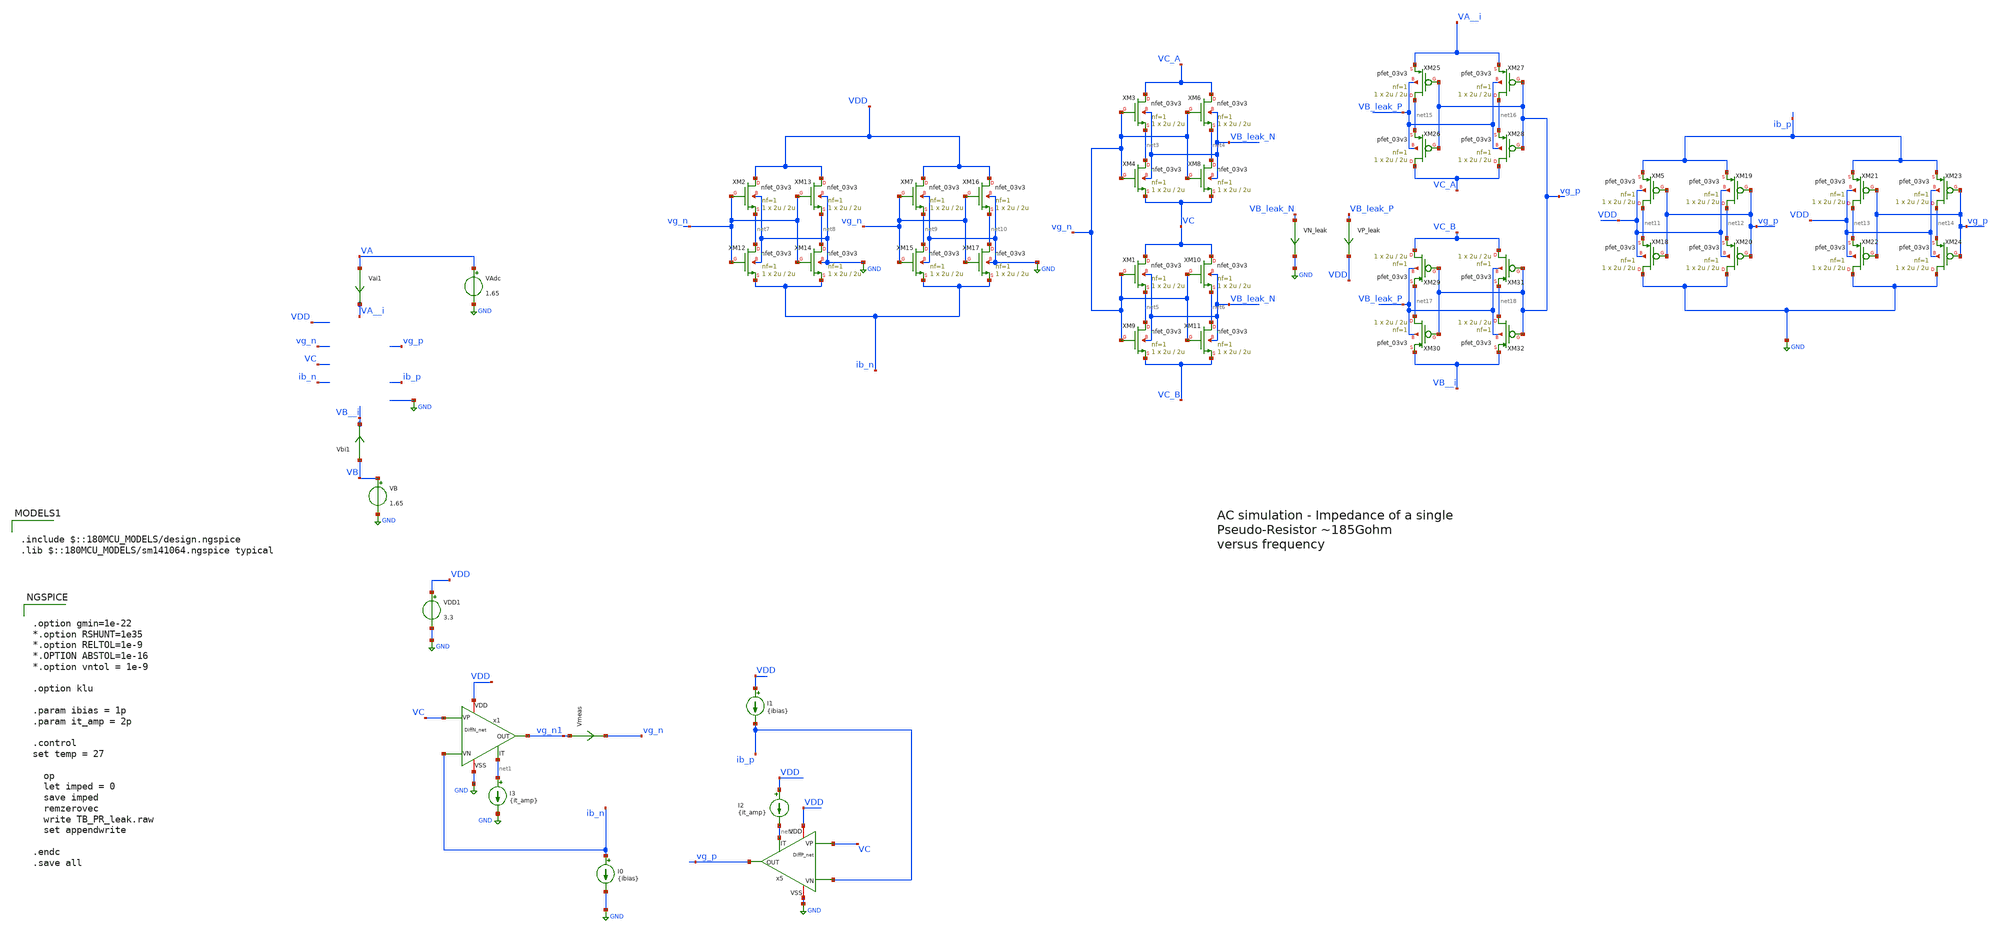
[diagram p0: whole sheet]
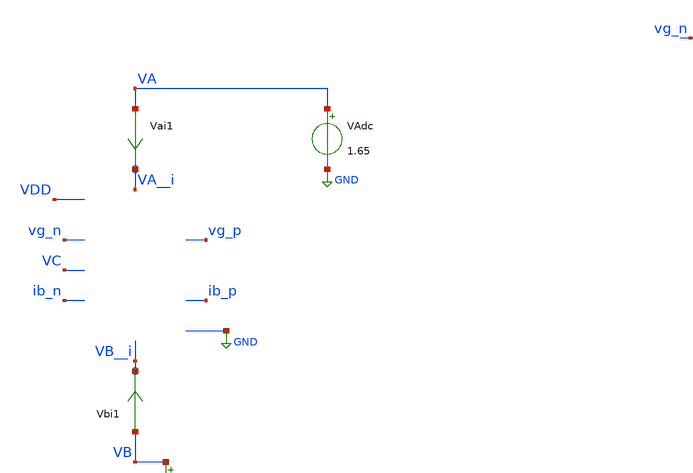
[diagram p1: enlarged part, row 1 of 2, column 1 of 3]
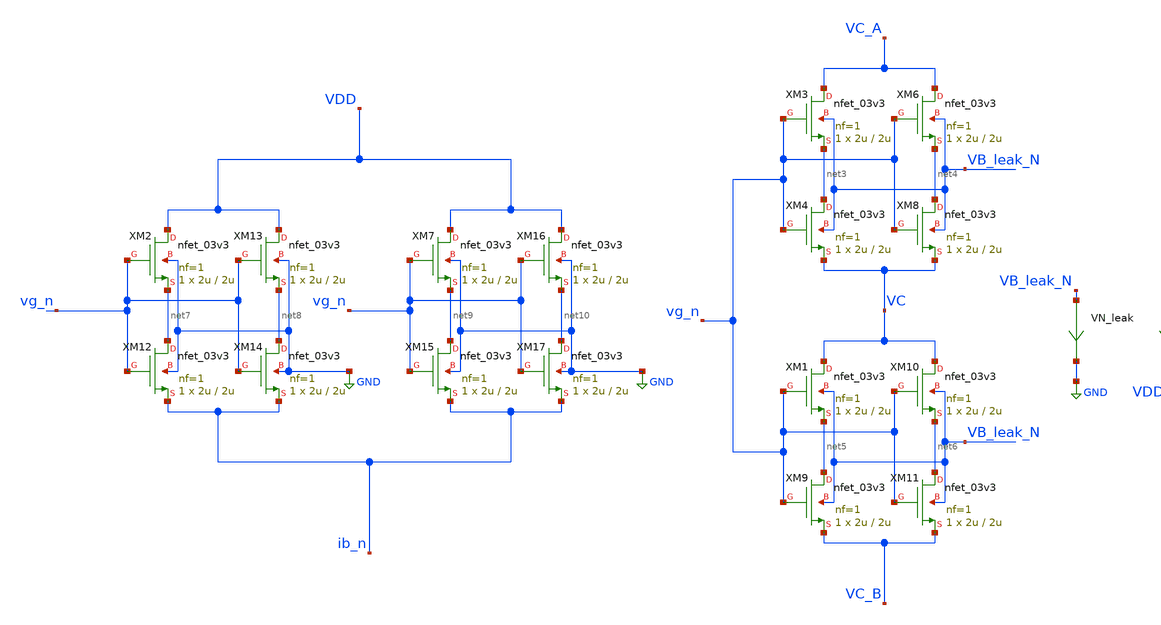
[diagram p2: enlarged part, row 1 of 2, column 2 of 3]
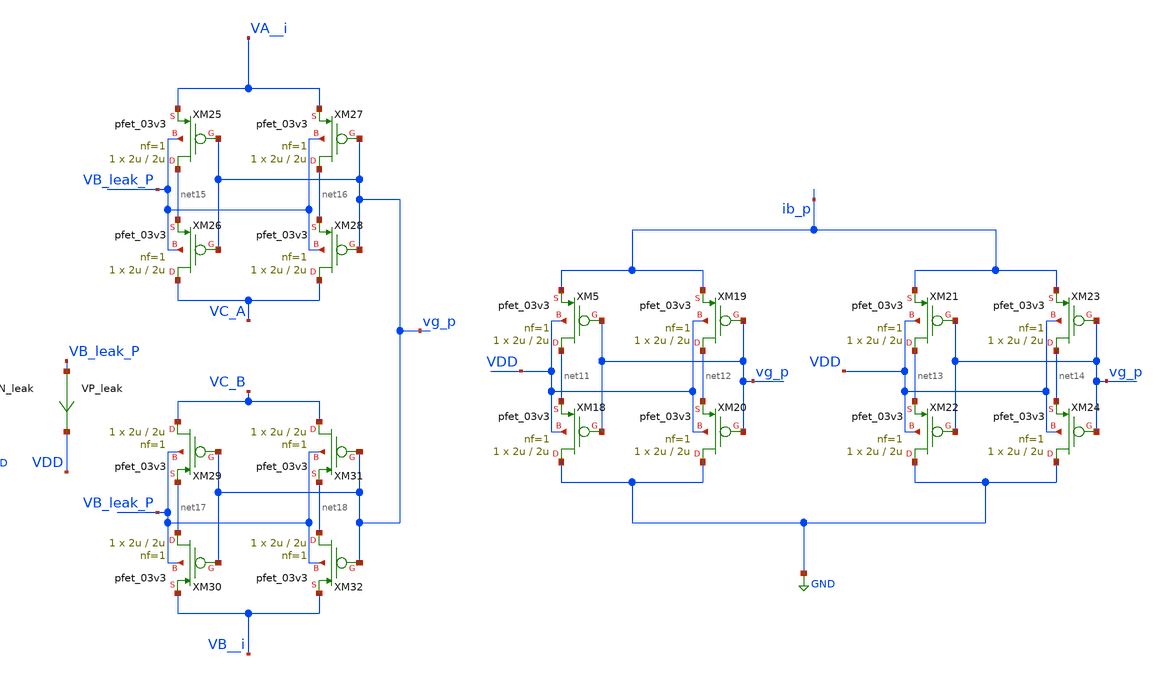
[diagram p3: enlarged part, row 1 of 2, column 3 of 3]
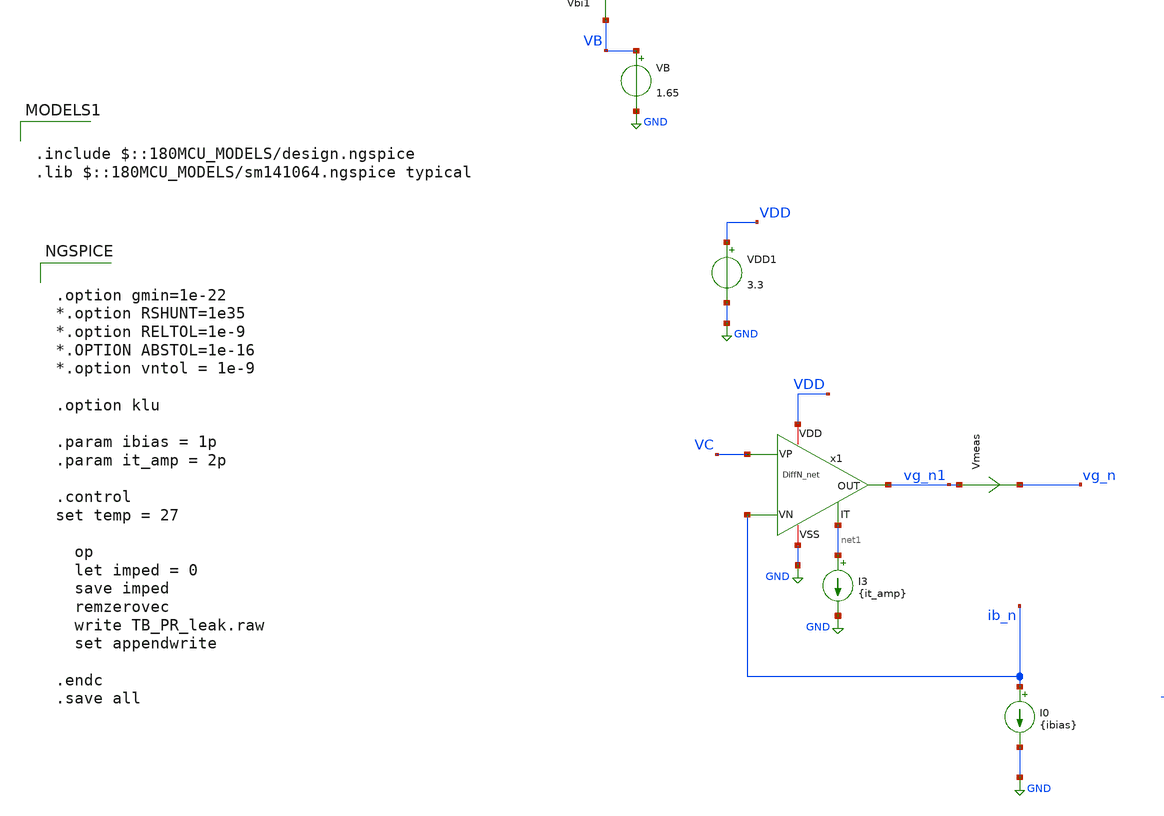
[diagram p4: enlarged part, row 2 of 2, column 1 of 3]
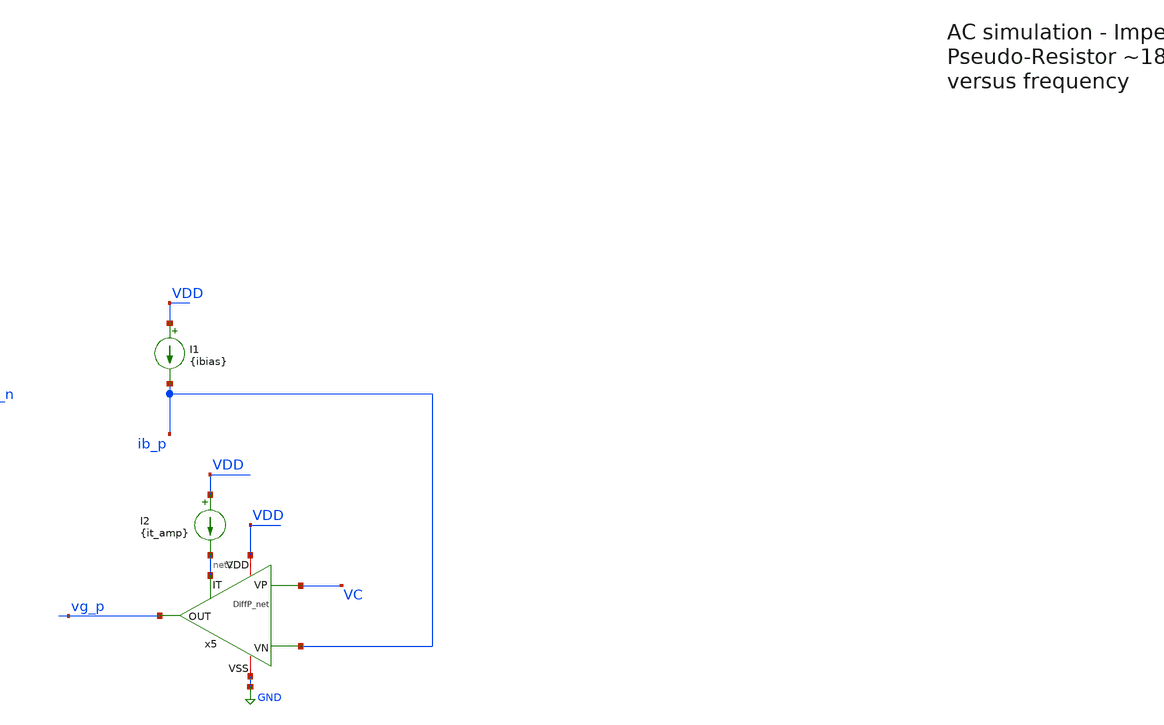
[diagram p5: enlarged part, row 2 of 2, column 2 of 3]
** sch_path: TIA_Filter/PseudoResistor/TB_PR_leak.sch
**.subckt TB_PR_leak
VDD1 VDD GND 3.3
VB VB GND 1.65
VAdc VA GND 1.65
Vai1 VA VA__i 0
.save i(vai1)
Vbi1 VB VB__i 0
.save i(vbi1)
I0 ib_n GND {ibias}
I1 VDD ib_p {ibias}
I2 VDD net2 {it_amp}
I3 net1 GND {it_amp}
x1 ib_n VC vg_n1 net1 VDD GND DiffN_net
x5 ib_p VC vg_p net2 VDD GND DiffP_net
XM3 VC_A vg_n net3 VB_leak_N nfet_03v3 L=2u W=2u nf=1 ad='int((nf+1)/2) * W/nf * 0.18u' as='int((nf+2)/2) * W/nf * 0.18u'
+ pd='2*int((nf+1)/2) * (W/nf + 0.18u)' ps='2*int((nf+2)/2) * (W/nf + 0.18u)' nrd='0.18u / W' nrs='0.18u / W'
+ sa=0 sb=0 sd=0 m=1
XM4 net3 vg_n VC VB_leak_N nfet_03v3 L=2u W=2u nf=1 ad='int((nf+1)/2) * W/nf * 0.18u' as='int((nf+2)/2) * W/nf * 0.18u'
+ pd='2*int((nf+1)/2) * (W/nf + 0.18u)' ps='2*int((nf+2)/2) * (W/nf + 0.18u)' nrd='0.18u / W' nrs='0.18u / W'
+ sa=0 sb=0 sd=0 m=1
XM6 VC_A vg_n net4 VB_leak_N nfet_03v3 L=2u W=2u nf=1 ad='int((nf+1)/2) * W/nf * 0.18u' as='int((nf+2)/2) * W/nf * 0.18u'
+ pd='2*int((nf+1)/2) * (W/nf + 0.18u)' ps='2*int((nf+2)/2) * (W/nf + 0.18u)' nrd='0.18u / W' nrs='0.18u / W'
+ sa=0 sb=0 sd=0 m=1
XM8 net4 vg_n VC VB_leak_N nfet_03v3 L=2u W=2u nf=1 ad='int((nf+1)/2) * W/nf * 0.18u' as='int((nf+2)/2) * W/nf * 0.18u'
+ pd='2*int((nf+1)/2) * (W/nf + 0.18u)' ps='2*int((nf+2)/2) * (W/nf + 0.18u)' nrd='0.18u / W' nrs='0.18u / W'
+ sa=0 sb=0 sd=0 m=1
XM1 VC vg_n net5 VB_leak_N nfet_03v3 L=2u W=2u nf=1 ad='int((nf+1)/2) * W/nf * 0.18u' as='int((nf+2)/2) * W/nf * 0.18u'
+ pd='2*int((nf+1)/2) * (W/nf + 0.18u)' ps='2*int((nf+2)/2) * (W/nf + 0.18u)' nrd='0.18u / W' nrs='0.18u / W'
+ sa=0 sb=0 sd=0 m=1
XM9 net5 vg_n VC_B VB_leak_N nfet_03v3 L=2u W=2u nf=1 ad='int((nf+1)/2) * W/nf * 0.18u' as='int((nf+2)/2) * W/nf * 0.18u'
+ pd='2*int((nf+1)/2) * (W/nf + 0.18u)' ps='2*int((nf+2)/2) * (W/nf + 0.18u)' nrd='0.18u / W' nrs='0.18u / W'
+ sa=0 sb=0 sd=0 m=1
XM10 VC vg_n net6 VB_leak_N nfet_03v3 L=2u W=2u nf=1 ad='int((nf+1)/2) * W/nf * 0.18u' as='int((nf+2)/2) * W/nf * 0.18u'
+ pd='2*int((nf+1)/2) * (W/nf + 0.18u)' ps='2*int((nf+2)/2) * (W/nf + 0.18u)' nrd='0.18u / W' nrs='0.18u / W'
+ sa=0 sb=0 sd=0 m=1
XM11 net6 vg_n VC_B VB_leak_N nfet_03v3 L=2u W=2u nf=1 ad='int((nf+1)/2) * W/nf * 0.18u' as='int((nf+2)/2) * W/nf * 0.18u'
+ pd='2*int((nf+1)/2) * (W/nf + 0.18u)' ps='2*int((nf+2)/2) * (W/nf + 0.18u)' nrd='0.18u / W' nrs='0.18u / W'
+ sa=0 sb=0 sd=0 m=1
XM2 VDD vg_n net7 GND nfet_03v3 L=2u W=2u nf=1 ad='int((nf+1)/2) * W/nf * 0.18u' as='int((nf+2)/2) * W/nf * 0.18u'
+ pd='2*int((nf+1)/2) * (W/nf + 0.18u)' ps='2*int((nf+2)/2) * (W/nf + 0.18u)' nrd='0.18u / W' nrs='0.18u / W'
+ sa=0 sb=0 sd=0 m=1
XM12 net7 vg_n ib_n GND nfet_03v3 L=2u W=2u nf=1 ad='int((nf+1)/2) * W/nf * 0.18u' as='int((nf+2)/2) * W/nf * 0.18u'
+ pd='2*int((nf+1)/2) * (W/nf + 0.18u)' ps='2*int((nf+2)/2) * (W/nf + 0.18u)' nrd='0.18u / W' nrs='0.18u / W'
+ sa=0 sb=0 sd=0 m=1
XM13 VDD vg_n net8 GND nfet_03v3 L=2u W=2u nf=1 ad='int((nf+1)/2) * W/nf * 0.18u' as='int((nf+2)/2) * W/nf * 0.18u'
+ pd='2*int((nf+1)/2) * (W/nf + 0.18u)' ps='2*int((nf+2)/2) * (W/nf + 0.18u)' nrd='0.18u / W' nrs='0.18u / W'
+ sa=0 sb=0 sd=0 m=1
XM14 net8 vg_n ib_n GND nfet_03v3 L=2u W=2u nf=1 ad='int((nf+1)/2) * W/nf * 0.18u' as='int((nf+2)/2) * W/nf * 0.18u'
+ pd='2*int((nf+1)/2) * (W/nf + 0.18u)' ps='2*int((nf+2)/2) * (W/nf + 0.18u)' nrd='0.18u / W' nrs='0.18u / W'
+ sa=0 sb=0 sd=0 m=1
XM7 VDD vg_n net9 GND nfet_03v3 L=2u W=2u nf=1 ad='int((nf+1)/2) * W/nf * 0.18u' as='int((nf+2)/2) * W/nf * 0.18u'
+ pd='2*int((nf+1)/2) * (W/nf + 0.18u)' ps='2*int((nf+2)/2) * (W/nf + 0.18u)' nrd='0.18u / W' nrs='0.18u / W'
+ sa=0 sb=0 sd=0 m=1
XM15 net9 vg_n ib_n GND nfet_03v3 L=2u W=2u nf=1 ad='int((nf+1)/2) * W/nf * 0.18u' as='int((nf+2)/2) * W/nf * 0.18u'
+ pd='2*int((nf+1)/2) * (W/nf + 0.18u)' ps='2*int((nf+2)/2) * (W/nf + 0.18u)' nrd='0.18u / W' nrs='0.18u / W'
+ sa=0 sb=0 sd=0 m=1
XM16 VDD vg_n net10 GND nfet_03v3 L=2u W=2u nf=1 ad='int((nf+1)/2) * W/nf * 0.18u' as='int((nf+2)/2) * W/nf * 0.18u'
+ pd='2*int((nf+1)/2) * (W/nf + 0.18u)' ps='2*int((nf+2)/2) * (W/nf + 0.18u)' nrd='0.18u / W' nrs='0.18u / W'
+ sa=0 sb=0 sd=0 m=1
XM17 net10 vg_n ib_n GND nfet_03v3 L=2u W=2u nf=1 ad='int((nf+1)/2) * W/nf * 0.18u' as='int((nf+2)/2) * W/nf * 0.18u'
+ pd='2*int((nf+1)/2) * (W/nf + 0.18u)' ps='2*int((nf+2)/2) * (W/nf + 0.18u)' nrd='0.18u / W' nrs='0.18u / W'
+ sa=0 sb=0 sd=0 m=1
XM5 net11 vg_p ib_p VDD pfet_03v3 L=2u W=2u nf=1 ad='int((nf+1)/2) * W/nf * 0.18u' as='int((nf+2)/2) * W/nf * 0.18u'
+ pd='2*int((nf+1)/2) * (W/nf + 0.18u)' ps='2*int((nf+2)/2) * (W/nf + 0.18u)' nrd='0.18u / W' nrs='0.18u / W'
+ sa=0 sb=0 sd=0 m=1
XM18 GND vg_p net11 VDD pfet_03v3 L=2u W=2u nf=1 ad='int((nf+1)/2) * W/nf * 0.18u' as='int((nf+2)/2) * W/nf * 0.18u'
+ pd='2*int((nf+1)/2) * (W/nf + 0.18u)' ps='2*int((nf+2)/2) * (W/nf + 0.18u)' nrd='0.18u / W' nrs='0.18u / W'
+ sa=0 sb=0 sd=0 m=1
XM19 net12 vg_p ib_p VDD pfet_03v3 L=2u W=2u nf=1 ad='int((nf+1)/2) * W/nf * 0.18u' as='int((nf+2)/2) * W/nf * 0.18u'
+ pd='2*int((nf+1)/2) * (W/nf + 0.18u)' ps='2*int((nf+2)/2) * (W/nf + 0.18u)' nrd='0.18u / W' nrs='0.18u / W'
+ sa=0 sb=0 sd=0 m=1
XM20 GND vg_p net12 VDD pfet_03v3 L=2u W=2u nf=1 ad='int((nf+1)/2) * W/nf * 0.18u' as='int((nf+2)/2) * W/nf * 0.18u'
+ pd='2*int((nf+1)/2) * (W/nf + 0.18u)' ps='2*int((nf+2)/2) * (W/nf + 0.18u)' nrd='0.18u / W' nrs='0.18u / W'
+ sa=0 sb=0 sd=0 m=1
XM21 net13 vg_p ib_p VDD pfet_03v3 L=2u W=2u nf=1 ad='int((nf+1)/2) * W/nf * 0.18u' as='int((nf+2)/2) * W/nf * 0.18u'
+ pd='2*int((nf+1)/2) * (W/nf + 0.18u)' ps='2*int((nf+2)/2) * (W/nf + 0.18u)' nrd='0.18u / W' nrs='0.18u / W'
+ sa=0 sb=0 sd=0 m=1
XM22 GND vg_p net13 VDD pfet_03v3 L=2u W=2u nf=1 ad='int((nf+1)/2) * W/nf * 0.18u' as='int((nf+2)/2) * W/nf * 0.18u'
+ pd='2*int((nf+1)/2) * (W/nf + 0.18u)' ps='2*int((nf+2)/2) * (W/nf + 0.18u)' nrd='0.18u / W' nrs='0.18u / W'
+ sa=0 sb=0 sd=0 m=1
XM23 net14 vg_p ib_p VDD pfet_03v3 L=2u W=2u nf=1 ad='int((nf+1)/2) * W/nf * 0.18u' as='int((nf+2)/2) * W/nf * 0.18u'
+ pd='2*int((nf+1)/2) * (W/nf + 0.18u)' ps='2*int((nf+2)/2) * (W/nf + 0.18u)' nrd='0.18u / W' nrs='0.18u / W'
+ sa=0 sb=0 sd=0 m=1
XM24 GND vg_p net14 VDD pfet_03v3 L=2u W=2u nf=1 ad='int((nf+1)/2) * W/nf * 0.18u' as='int((nf+2)/2) * W/nf * 0.18u'
+ pd='2*int((nf+1)/2) * (W/nf + 0.18u)' ps='2*int((nf+2)/2) * (W/nf + 0.18u)' nrd='0.18u / W' nrs='0.18u / W'
+ sa=0 sb=0 sd=0 m=1
XM25 net15 vg_p VA__i VB_leak_P pfet_03v3 L=2u W=2u nf=1 ad='int((nf+1)/2) * W/nf * 0.18u' as='int((nf+2)/2) * W/nf * 0.18u'
+ pd='2*int((nf+1)/2) * (W/nf + 0.18u)' ps='2*int((nf+2)/2) * (W/nf + 0.18u)' nrd='0.18u / W' nrs='0.18u / W'
+ sa=0 sb=0 sd=0 m=1
XM26 VC_A vg_p net15 VB_leak_P pfet_03v3 L=2u W=2u nf=1 ad='int((nf+1)/2) * W/nf * 0.18u' as='int((nf+2)/2) * W/nf * 0.18u'
+ pd='2*int((nf+1)/2) * (W/nf + 0.18u)' ps='2*int((nf+2)/2) * (W/nf + 0.18u)' nrd='0.18u / W' nrs='0.18u / W'
+ sa=0 sb=0 sd=0 m=1
XM27 net16 vg_p VA__i VB_leak_P pfet_03v3 L=2u W=2u nf=1 ad='int((nf+1)/2) * W/nf * 0.18u' as='int((nf+2)/2) * W/nf * 0.18u'
+ pd='2*int((nf+1)/2) * (W/nf + 0.18u)' ps='2*int((nf+2)/2) * (W/nf + 0.18u)' nrd='0.18u / W' nrs='0.18u / W'
+ sa=0 sb=0 sd=0 m=1
XM28 VC_A vg_p net16 VB_leak_P pfet_03v3 L=2u W=2u nf=1 ad='int((nf+1)/2) * W/nf * 0.18u' as='int((nf+2)/2) * W/nf * 0.18u'
+ pd='2*int((nf+1)/2) * (W/nf + 0.18u)' ps='2*int((nf+2)/2) * (W/nf + 0.18u)' nrd='0.18u / W' nrs='0.18u / W'
+ sa=0 sb=0 sd=0 m=1
XM29 VC_B vg_p net17 VB_leak_P pfet_03v3 L=2u W=2u nf=1 ad='int((nf+1)/2) * W/nf * 0.18u' as='int((nf+2)/2) * W/nf * 0.18u'
+ pd='2*int((nf+1)/2) * (W/nf + 0.18u)' ps='2*int((nf+2)/2) * (W/nf + 0.18u)' nrd='0.18u / W' nrs='0.18u / W'
+ sa=0 sb=0 sd=0 m=1
XM30 net17 vg_p VB__i VB_leak_P pfet_03v3 L=2u W=2u nf=1 ad='int((nf+1)/2) * W/nf * 0.18u' as='int((nf+2)/2) * W/nf * 0.18u'
+ pd='2*int((nf+1)/2) * (W/nf + 0.18u)' ps='2*int((nf+2)/2) * (W/nf + 0.18u)' nrd='0.18u / W' nrs='0.18u / W'
+ sa=0 sb=0 sd=0 m=1
XM31 VC_B vg_p net18 VB_leak_P pfet_03v3 L=2u W=2u nf=1 ad='int((nf+1)/2) * W/nf * 0.18u' as='int((nf+2)/2) * W/nf * 0.18u'
+ pd='2*int((nf+1)/2) * (W/nf + 0.18u)' ps='2*int((nf+2)/2) * (W/nf + 0.18u)' nrd='0.18u / W' nrs='0.18u / W'
+ sa=0 sb=0 sd=0 m=1
XM32 net18 vg_p VB__i VB_leak_P pfet_03v3 L=2u W=2u nf=1 ad='int((nf+1)/2) * W/nf * 0.18u' as='int((nf+2)/2) * W/nf * 0.18u'
+ pd='2*int((nf+1)/2) * (W/nf + 0.18u)' ps='2*int((nf+2)/2) * (W/nf + 0.18u)' nrd='0.18u / W' nrs='0.18u / W'
+ sa=0 sb=0 sd=0 m=1
VN_leak VB_leak_N GND 0
.save i(vn_leak)
VP_leak VB_leak_P VDD 0
.save i(vp_leak)
Vmeas vg_n1 vg_n 0
.save i(vmeas)
**** begin user architecture code


.option gmin=1e-22
*.option RSHUNT=1e35
*.option RELTOL=1e-9
*.OPTION ABSTOL=1e-16
*.option vntol = 1e-9

.option klu

.param ibias = 1p
.param it_amp = 2p

.control
set temp = 27

  op
  let imped = 0
  save imped
  remzerovec
  write TB_PR_leak.raw
  set appendwrite

.endc
.save all



.include $::180MCU_MODELS/design.ngspice
.lib $::180MCU_MODELS/sm141064.ngspice typical


**** end user architecture code
**.ends
.GLOBAL GND
.end
